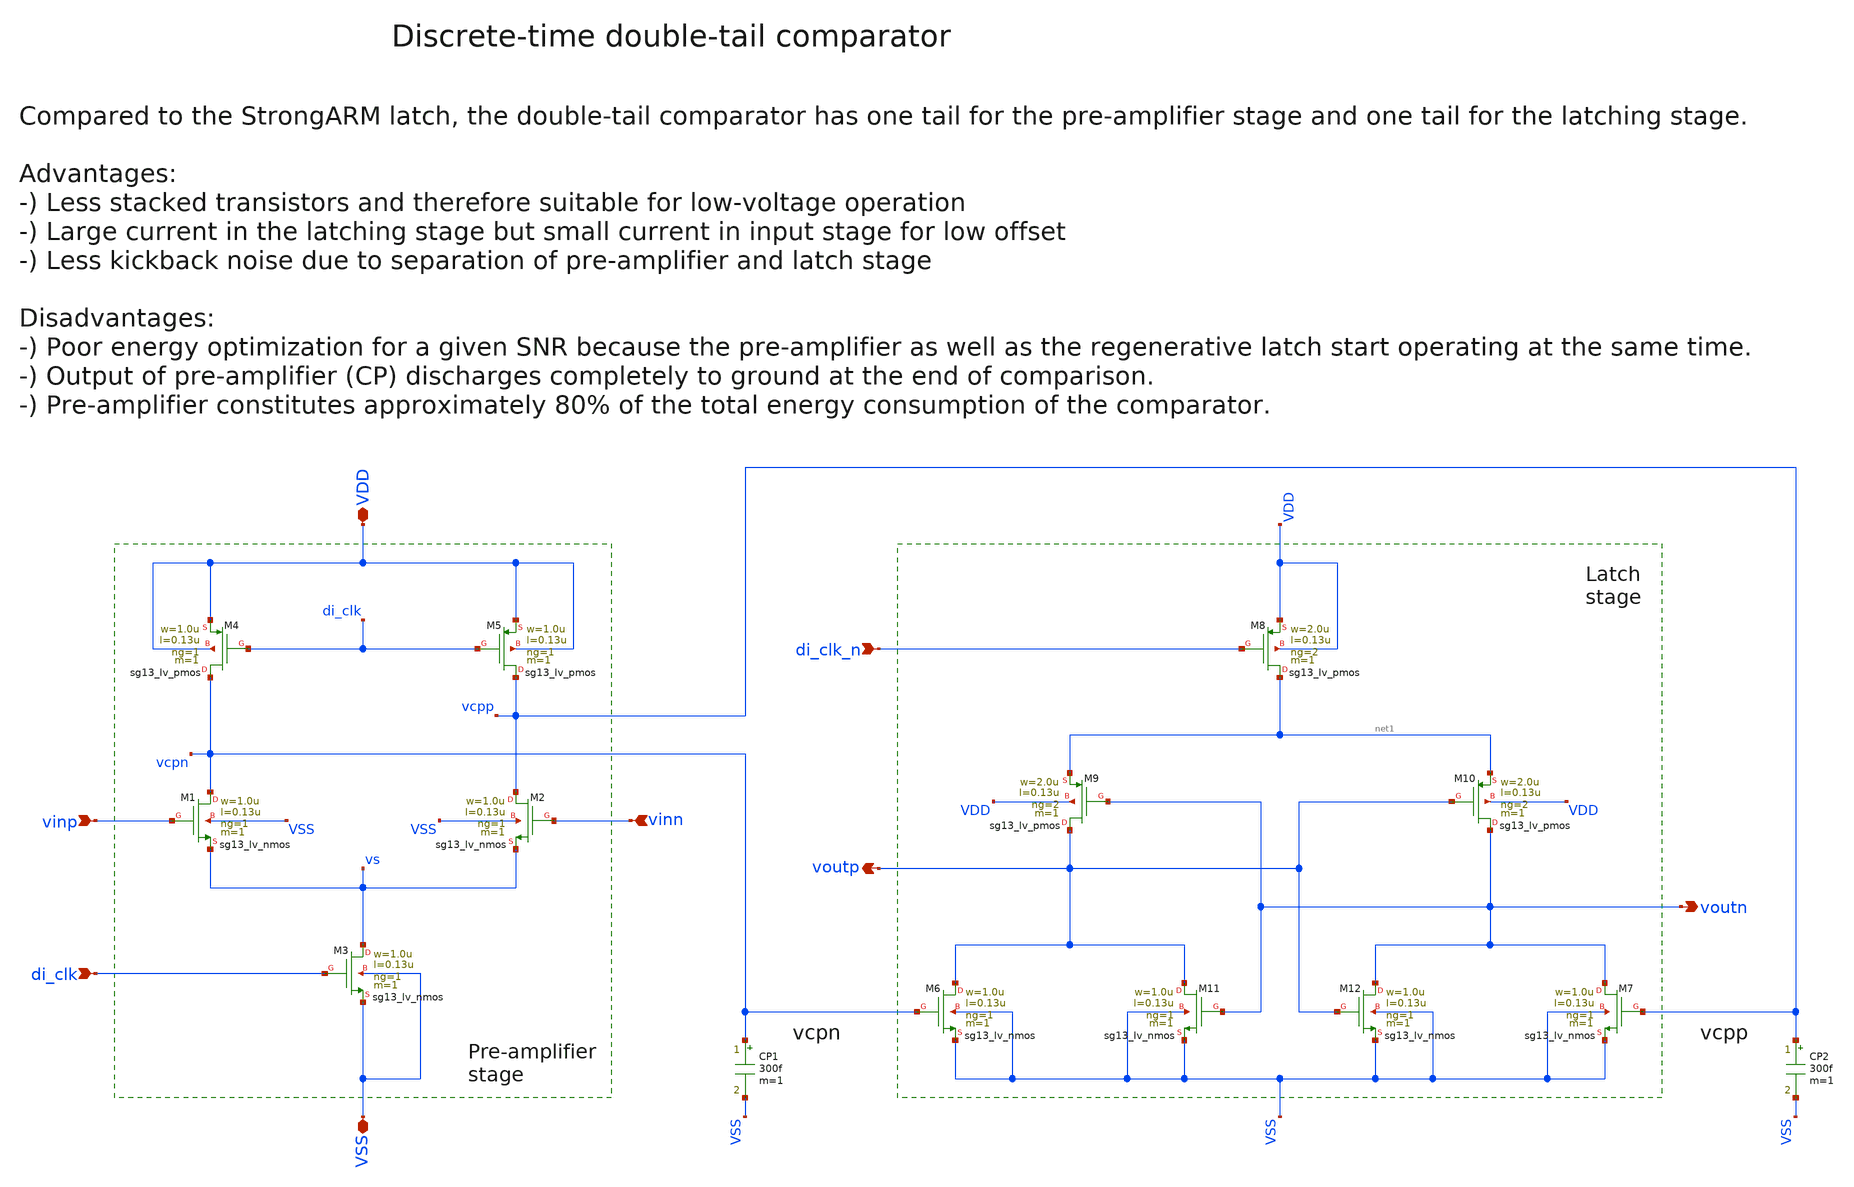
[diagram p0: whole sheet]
** sch_path: SG13G2_ATBS-ADC-main/xschem/comparator/discrete_time/Double-tail/double_tail_comparator.sch
**.subckt double_tail_comparator voutp voutn di_clk_n VDD VSS vinp vinn di_clk
*.opin voutp
*.opin voutn
*.ipin di_clk_n
*.iopin VDD
*.iopin VSS
*.ipin vinp
*.ipin vinn
*.ipin di_clk
XM6 voutp vcpn VSS VSS sg13_lv_nmos w=1.0u l=0.13u ng=1 m=1 mm_ok=1
XM8 net1 di_clk_n VDD VDD sg13_lv_pmos w=2.0u l=0.13u ng=2 m=1 mm_ok=1
XM9 voutp voutn net1 VDD sg13_lv_pmos w=2.0u l=0.13u ng=2 m=1 mm_ok=1
XM10 voutn voutp net1 VDD sg13_lv_pmos w=2.0u l=0.13u ng=2 m=1 mm_ok=1
XM11 voutp voutn VSS VSS sg13_lv_nmos w=1.0u l=0.13u ng=1 m=1 mm_ok=1
XM12 voutn voutp VSS VSS sg13_lv_nmos w=1.0u l=0.13u ng=1 m=1 mm_ok=1
XM7 voutn vcpp VSS VSS sg13_lv_nmos w=1.0u l=0.13u ng=1 m=1 mm_ok=1
CP1 vcpn VSS 300f m=1
CP2 vcpp VSS 300f m=1
XM1 vcpn vinp vs VSS sg13_lv_nmos w=1.0u l=0.13u ng=1 m=1 mm_ok=1
XM2 vcpp vinn vs VSS sg13_lv_nmos w=1.0u l=0.13u ng=1 m=1 mm_ok=1
XM3 vs di_clk VSS VSS sg13_lv_nmos w=1.0u l=0.13u ng=1 m=1 mm_ok=1
XM4 vcpn di_clk VDD VDD sg13_lv_pmos w=1.0u l=0.13u ng=1 m=1 mm_ok=1
XM5 vcpp di_clk VDD VDD sg13_lv_pmos w=1.0u l=0.13u ng=1 m=1 mm_ok=1
**.ends
.end
